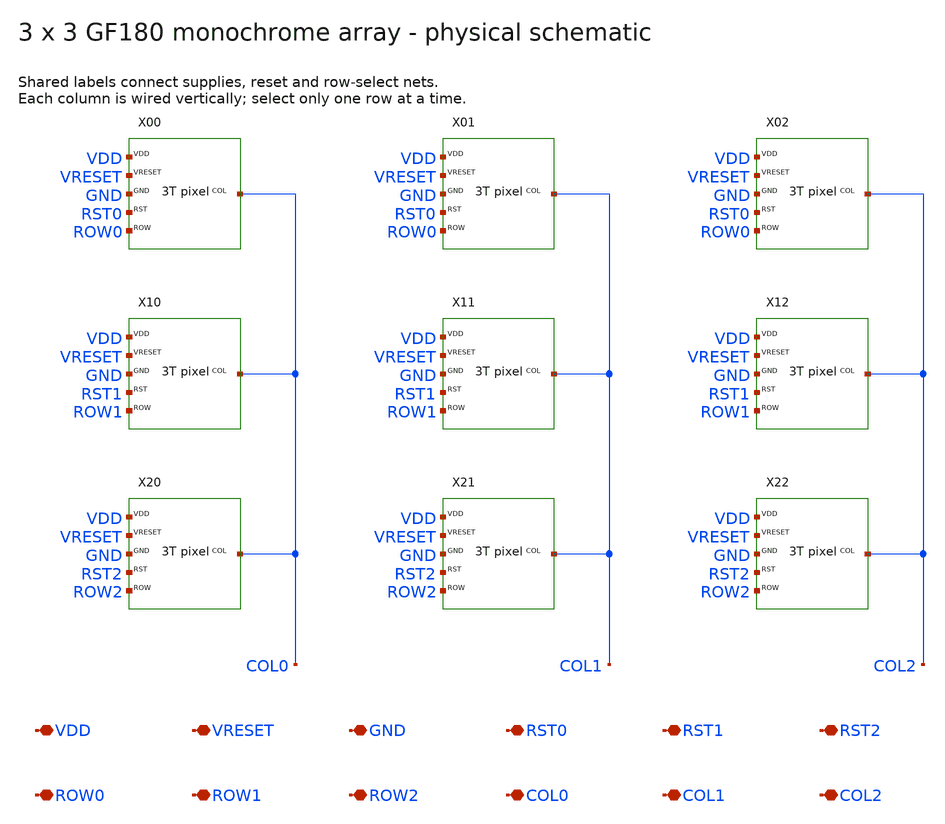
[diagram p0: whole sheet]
** sch_path: xschem/array_3x3.sch
**.subckt array_3x3 VDD VRESET GND RST0 RST1 RST2 ROW0 ROW1 ROW2 COL0 COL1 COL2
*.iopin VDD
*.iopin VRESET
*.iopin GND
*.iopin RST0
*.iopin RST1
*.iopin RST2
*.iopin ROW0
*.iopin ROW1
*.iopin ROW2
*.iopin COL0
*.iopin COL1
*.iopin COL2
X00 VDD VRESET GND RST0 ROW0 COL0 pixel_physical
X01 VDD VRESET GND RST0 ROW0 COL1 pixel_physical
X02 VDD VRESET GND RST0 ROW0 COL2 pixel_physical
X10 VDD VRESET GND RST1 ROW1 COL0 pixel_physical
X11 VDD VRESET GND RST1 ROW1 COL1 pixel_physical
X12 VDD VRESET GND RST1 ROW1 COL2 pixel_physical
X20 VDD VRESET GND RST2 ROW2 COL0 pixel_physical
X21 VDD VRESET GND RST2 ROW2 COL1 pixel_physical
X22 VDD VRESET GND RST2 ROW2 COL2 pixel_physical
**.ends

* expanding   symbol:  pixel_physical.sym # of pins=6
** sym_path: xschem/pixel_physical.sym
** sch_path: xschem/pixel_physical.sch
.subckt pixel_physical VDD VRESET GND RST ROW COL
*.iopin VDD
*.iopin VRESET
*.iopin GND
*.iopin RST
*.iopin ROW
*.iopin COL
Xrst VRESET RST sense GND nfet_03v3 L=0.5u W=1u nf=1 ad=0.44p as=0.44p pd=2.88u ps=2.88u nrd=0 nrs=0
+ sa=0 sb=0 sd=0 m=1
Xsf VDD sense sf GND nfet_03v3 L=0.5u W=1u nf=1 ad=0.44p as=0.44p pd=2.88u ps=2.88u nrd=0 nrs=0 sa=0
+ sb=0 sd=0 m=1
Xsel sf ROW COL GND nfet_03v3 L=0.5u W=1u nf=1 ad=0.44p as=0.44p pd=2.88u ps=2.88u nrd=0 nrs=0 sa=0
+ sb=0 sd=0 m=1
Dphoto GND sense diode_nd2ps_03v3 area='5u * 5u ' pj='2*5u + 2*5u ' m=1
.ends

.end
